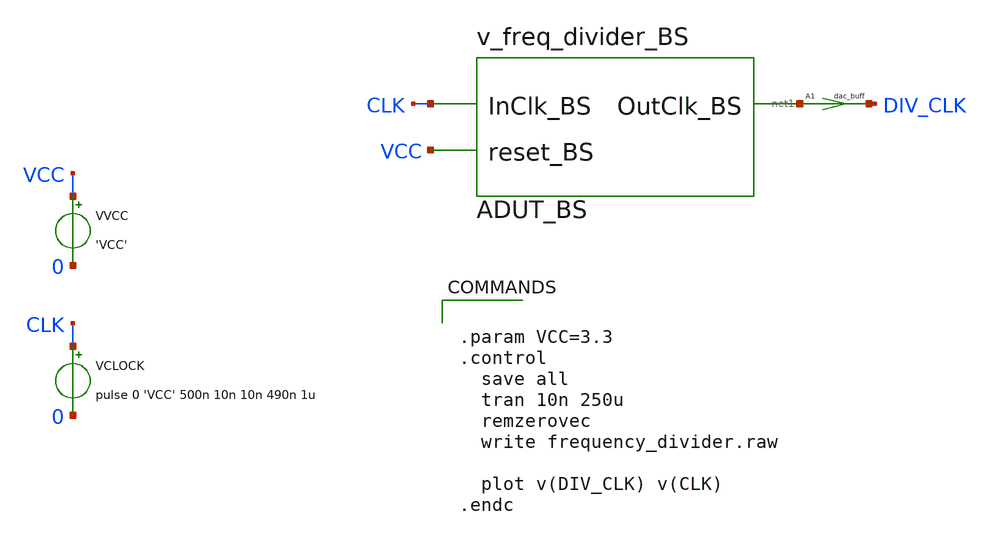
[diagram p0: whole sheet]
** sch_path: sch/design/frequency_divider_BS.sch
**.subckt frequency_divider_BS
VVCC VCC 0 'VCC'
VCLOCK CLK 0 pulse 0 'VCC' 500n 10n 10n 490n 1u
A1 [ net1 ] [ DIV_CLK ] dac_buff
ADUT_BS [ CLK VCC ] [ net1 ] dut_BS
**** begin user architecture code


.param VCC=3.3
.control
  save all
  tran 10n 250u
  remzerovec
  write frequency_divider.raw

  plot v(DIV_CLK) v(CLK)
.endc


**** end user architecture code
**.ends
**** begin user architecture code
.model dac_buff dac_bridge input_load=1e-15 t_rise=10n t_fall=10n  out_low=0 out_high=3.3
.model dut_BS d_cosim simulation="ivlng" sim_args=["freq_divider_BS"]   vlow=0.8 vhigh=2.0   v0=0
+ v1=3.3   rise=1n fall=1n
**** end user architecture code
.end
